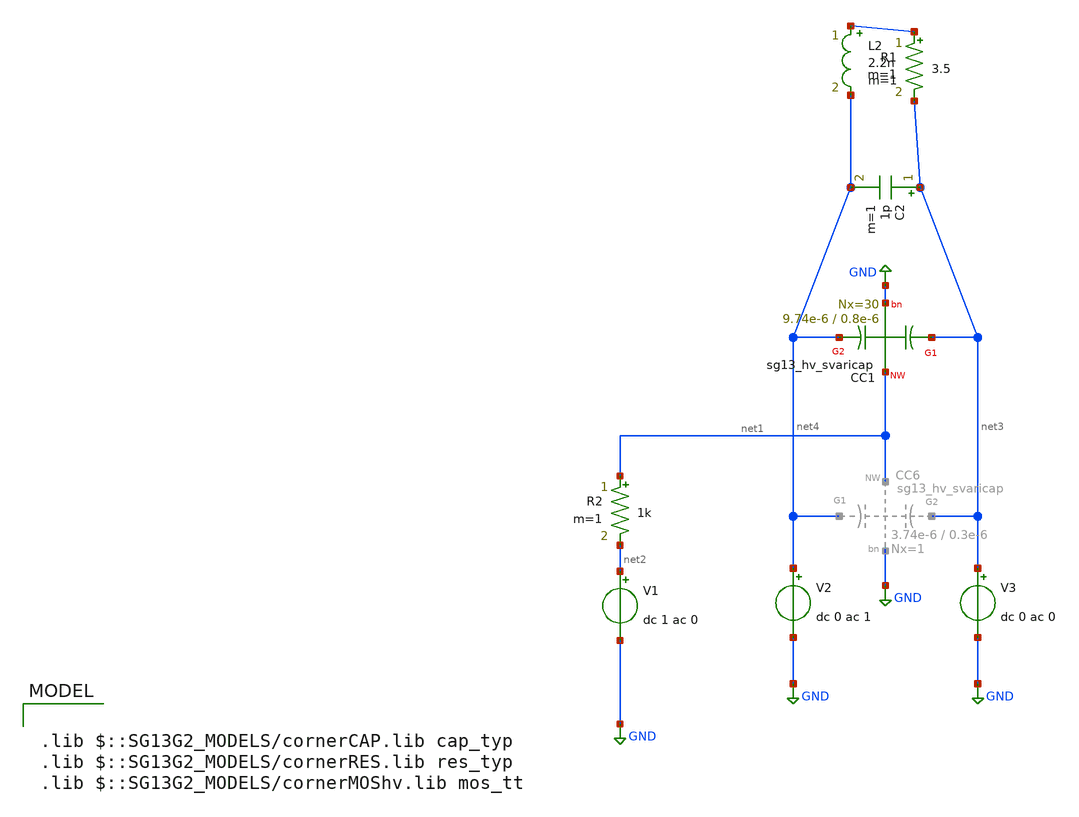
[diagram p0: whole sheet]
** sch_path: design_data/xschem/measuremenst_and_test_of_idas/ac_svaricap_test7.sch
**.subckt ac_svaricap_test7
V1 net2 GND dc 1 ac 0
V3 net3 GND dc 0 ac 0
V2 net4 GND dc 0 ac 1
XC1 net3 net1 net4 GND sg13_hv_svaricap w=9.74e-6 l=0.8e-6 Nx=30
C2 net3 net4 1p m=1
R1 net5 net3 3.5 m=1
L2 net5 net4 2.2n m=1
R2 net1 net2 1k m=1
**** begin user architecture code

.lib $::SG13G2_MODELS/cornerCAP.lib cap_typ
.lib $::SG13G2_MODELS/cornerRES.lib res_typ
.lib $::SG13G2_MODELS/cornerMOShv.lib mos_tt



*.param temp=27

.control
save all


op
write
set appendwrite

let vfreq = 0
while vfreq < 1.8
   alter v1 = vfreq
   ac lin 1000 .1GHz 10GHz
   let I1=(i(V3))
   let Ctot=imag(I1)/(2*3.1415*frequency)
   let Q=imag(I1)/real(I1)
   write
   set appendwrite

   let vfreq = vfreq + 0.1
end

   alter v1 = 1.8
   ac lin 1000 .1GHz 10GHz
   let I1=(i(V3))
   let Ctot=imag(I1)/(2*3.1415*frequency)
   let Q=imag(I1)/real(I1)
   write
   set appendwrite

   alter c2 = 300f
   ac lin 1000 .1GHz 10GHz
   let I1=(i(V3))
   let Ctot=imag(I1)/(2*3.1415*frequency)
   let Q=imag(I1)/real(I1)
   write
   set appendwrite


   alter c2 = 1f
   ac lin 1000 .1GHz 10GHz
   let I1=(i(V3))
   let Ctot=imag(I1)/(2*3.1415*frequency)
   let Q=imag(I1)/real(I1)
   write
   set appendwrite

   alter c1 nx = 30
   ac lin 1000 .1GHz 10GHz
   let I1=(i(V3))
   let Ctot=imag(I1)/(2*3.1415*frequency)
   let Q=imag(I1)/real(I1)
   write
   set appendwrite


*quit
.endc


**** end user architecture code
**.ends
.GLOBAL GND
.end
